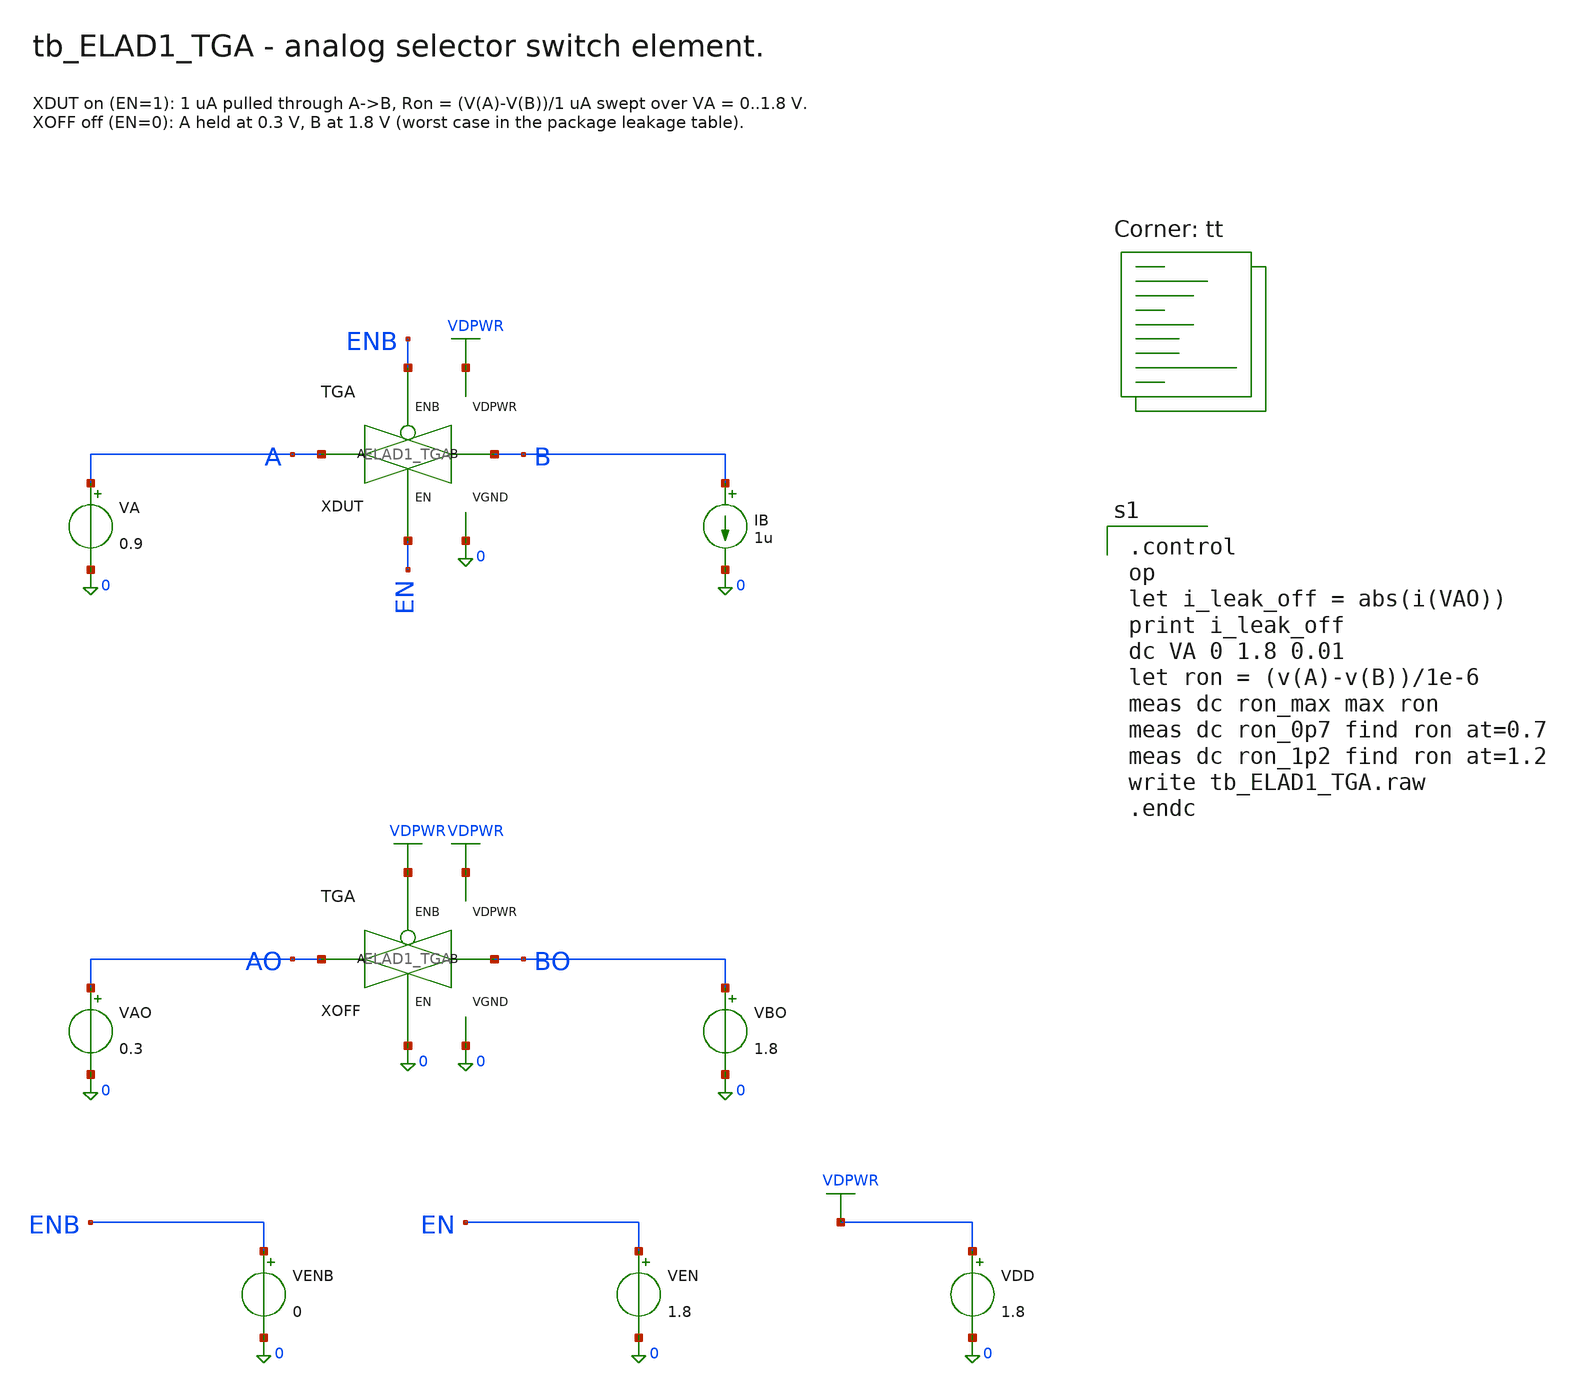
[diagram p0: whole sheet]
** sch_path: cells/ELAD1_TGA/schematic/tb_ELAD1_TGA.sch
**.subckt tb_ELAD1_TGA
XDUT A B EN ENB VDPWR 0 ELAD1_TGA
VA A 0 0.9
IB B 0 1u
XOFF AO BO 0 VDPWR VDPWR 0 ELAD1_TGA
VAO AO 0 0.3
VBO BO 0 1.8
VENB ENB 0 0
VEN EN 0 1.8
VDD VDPWR 0 1.8
**** begin user architecture code

.control
op
let i_leak_off = abs(i(VAO))
print i_leak_off
dc VA 0 1.8 0.01
let ron = (v(A)-v(B))/1e-6
meas dc ron_max max ron
meas dc ron_0p7 find ron at=0.7
meas dc ron_1p2 find ron at=1.2
write tb_ELAD1_TGA.raw
.endc

.lib $::SKYWATER_MODELS/sky130.lib.spice tt
**** end user architecture code
**.ends

* expanding   symbol:  ELAD1_TGA.sym # of pins=6
** sym_path: cells/ELAD1_TGA/schematic/ELAD1_TGA.sym
** sch_path: cells/ELAD1_TGA/schematic/ELAD1_TGA.sch
.subckt ELAD1_TGA A B EN ENB VDPWR VGND
*.iopin A
*.iopin B
*.iopin EN
*.iopin ENB
*.iopin VDPWR
*.iopin VGND
XMN A EN B VGND sky130_fd_pr__nfet_01v8_lvt L=0.15 W=4 nf=1 ad='int((1 + 1)/2) * 4 / 1 * 0.29' as='int((1 + 2)/2) * 4 / 1 * 0.29'
+ pd='2*int((1 + 1)/2) * (4 / 1 + 0.29)' ps='2*int((1 + 2)/2) * (4 / 1 + 0.29)' nrd='0.29 / 4 ' nrs='0.29 / 4 '
+ sa=0 sb=0 sd=0 mult=1 m=1
XMP A ENB B VDPWR sky130_fd_pr__pfet_01v8_lvt L=0.35 W=12 nf=1 ad='int((1 + 1)/2) * 12 / 1 * 0.29' as='int((1 + 2)/2) * 12 / 1 * 0.29'
+ pd='2*int((1 + 1)/2) * (12 / 1 + 0.29)' ps='2*int((1 + 2)/2) * (12 / 1 + 0.29)' nrd='0.29 / 12 ' nrs='0.29 / 12 '
+ sa=0 sb=0 sd=0 mult=1 m=1
.ends

.end
